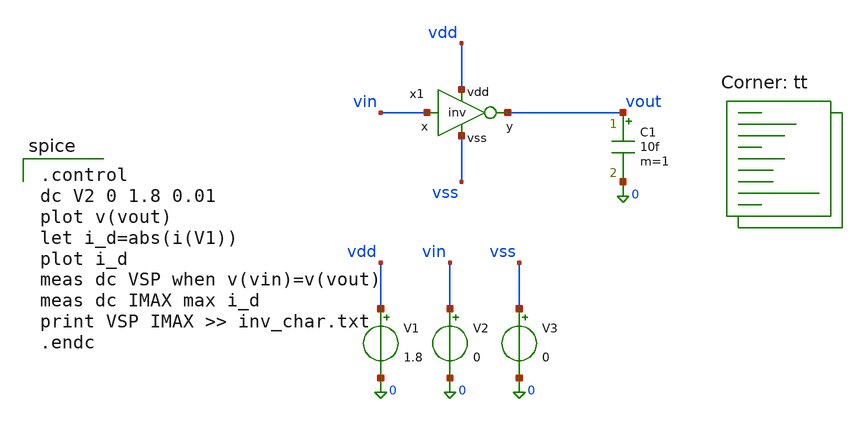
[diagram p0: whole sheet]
** sch_path: xschem/inv/sim_inv.sch
**.subckt sim_inv
x1 vdd vin vout vss inv
V1 vdd 0 1.8
V2 vin 0 0
V3 vss 0 0
C1 vout 0 10f m=1
**** begin user architecture code
.lib $::SKYWATER_MODELS/sky130.lib.spice tt

.control
dc V2 0 1.8 0.01
plot v(vout)
let i_d=abs(i(V1))
plot i_d
meas dc VSP when v(vin)=v(vout)
meas dc IMAX max i_d
print VSP IMAX >> inv_char.txt
.endc

**** end user architecture code
**.ends

* expanding   symbol:  inv.sym # of pins=4
** sym_path: xschem/inv/inv.sym
** sch_path: xschem/inv/inv.sch
.subckt inv vdd x y vss
*.ipin vdd
*.ipin vss
*.ipin x
*.opin y
XM1 y x vdd vdd sky130_fd_pr__pfet_01v8_lvt L=0.5 W=1.2 nf=1 ad='int((1 + 1)/2) * 1.2 / 1 * 0.29' as='int((1 + 2)/2) * 1.2 / 1 * 0.29'
+ pd='2*int((1 + 1)/2) * (1.2 / 1 + 0.29)' ps='2*int((1 + 2)/2) * (1.2 / 1 + 0.29)' nrd='0.29 / 1.2 ' nrs='0.29 / 1.2 '
+ sa=0 sb=0 sd=0 mult=1 m=1
XM2 y x vss vss sky130_fd_pr__nfet_01v8_lvt L=0.5 W=0.5 nf=1 ad='int((1 + 1)/2) * 0.5 / 1 * 0.29' as='int((1 + 2)/2) * 0.5 / 1 * 0.29'
+ pd='2*int((1 + 1)/2) * (0.5 / 1 + 0.29)' ps='2*int((1 + 2)/2) * (0.5 / 1 + 0.29)' nrd='0.29 / 0.5 ' nrs='0.29 / 0.5 '
+ sa=0 sb=0 sd=0 mult=1 m=1
.ends

.end
